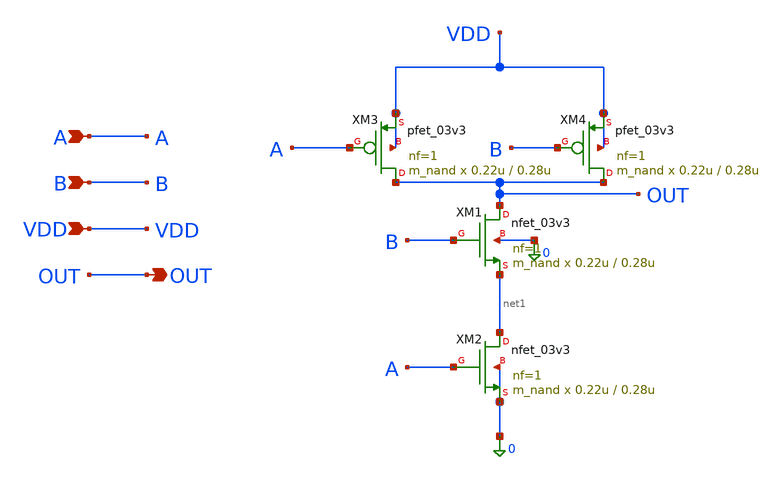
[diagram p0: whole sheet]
** sch_path: Design_Files/IC Design/Schematic/SAR_ADC_BLOCKS/NAND/NAND.sch
**.subckt NAND A B VDD OUT
*.ipin A
*.ipin B
*.ipin VDD
*.opin OUT
XM1 OUT B net1 0 nfet_03v3 L=0.28u W=0.22u nf=1 ad='int((nf+1)/2) * W/nf * 0.18u' as='int((nf+2)/2) * W/nf * 0.18u'
+ pd='2*int((nf+1)/2) * (W/nf + 0.18u)' ps='2*int((nf+2)/2) * (W/nf + 0.18u)' nrd='0.18u / W' nrs='0.18u / W'
+ sa=0 sb=0 sd=0 m=m_nand
XM2 net1 A 0 0 nfet_03v3 L=0.28u W=0.22u nf=1 ad='int((nf+1)/2) * W/nf * 0.18u' as='int((nf+2)/2) * W/nf * 0.18u'
+ pd='2*int((nf+1)/2) * (W/nf + 0.18u)' ps='2*int((nf+2)/2) * (W/nf + 0.18u)' nrd='0.18u / W' nrs='0.18u / W'
+ sa=0 sb=0 sd=0 m=m_nand
XM3 OUT A VDD VDD pfet_03v3 L=0.28u W=0.22u nf=1 ad='int((nf+1)/2) * W/nf * 0.18u' as='int((nf+2)/2) * W/nf * 0.18u'
+ pd='2*int((nf+1)/2) * (W/nf + 0.18u)' ps='2*int((nf+2)/2) * (W/nf + 0.18u)' nrd='0.18u / W' nrs='0.18u / W'
+ sa=0 sb=0 sd=0 m=m_nand
XM4 OUT B VDD VDD pfet_03v3 L=0.28u W=0.22u nf=1 ad='int((nf+1)/2) * W/nf * 0.18u' as='int((nf+2)/2) * W/nf * 0.18u'
+ pd='2*int((nf+1)/2) * (W/nf + 0.18u)' ps='2*int((nf+2)/2) * (W/nf + 0.18u)' nrd='0.18u / W' nrs='0.18u / W'
+ sa=0 sb=0 sd=0 m=m_nand
**.ends
.end
